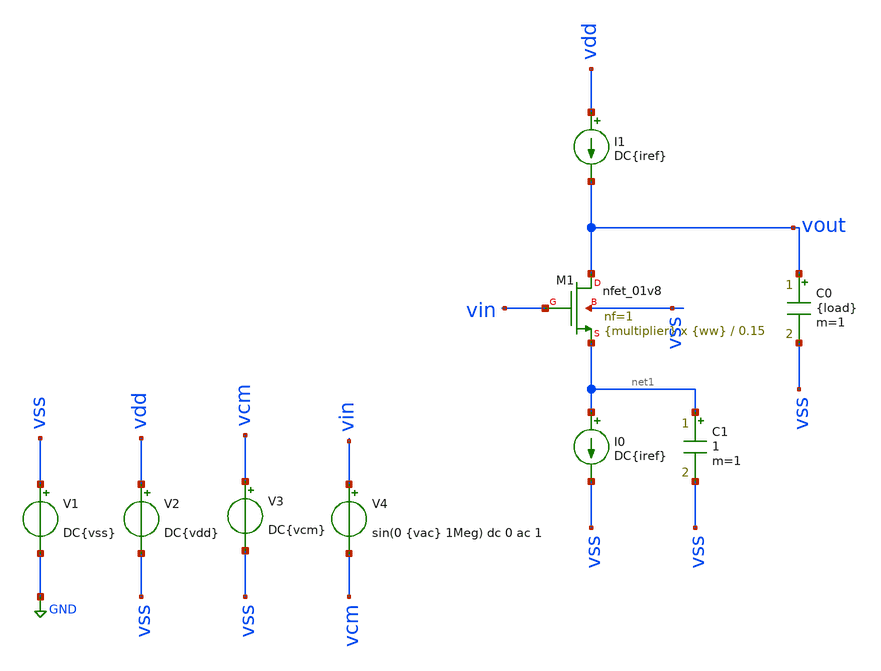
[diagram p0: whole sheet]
** sch_path: tp4/tp4.sch
**.subckt tp4
V1 vss GND DC{vss}
V2 vdd vss DC{vdd}
V3 vcm vss DC{vcm}
V4 vin vcm sin(0 {vac} 1Meg) dc 0 ac 1
XM1 vout vin net1 vss sky130_fd_pr__nfet_01v8 L=0.15 W={ww} nf=1 ad='int((nf+1)/2) * W/nf * 0.29' as='int((nf+2)/2) * W/nf * 0.29'
+ pd='2*int((nf+1)/2) * (W/nf + 0.29)' ps='2*int((nf+2)/2) * (W/nf + 0.29)' nrd='0.29 / W' nrs='0.29 / W'
+ sa=0 sb=0 sd=0 mult={multiplier} m={multiplier}
I0 net1 vss DC{iref}
C0 vout vss {load} m=1
I1 vdd vout DC{iref}
C1 net1 vss 1 m=1
**** begin user architecture code



* Circuit Parameters
.param iref = 100u
.param vdd  = 1.8
.param vss  = 0.0
.param vcm  = 0.9
.param vac  = 10m
.param multiplier = 1
.param load = 0.001f
.param ww = 0.45
.options TEMP = 65.0


* Models
*.lib ~/skywater/skywater-pdk/libraries/sky130_fd_pr_ngspice/latest/models/corners/sky130.lib TT
*.lib ~/skywater/skywater-pdk/libraries/sky130_fd_pr_ngspice/latest/models/corners/sky130.lib TT
.lib /foss/pdks/sky130A/libs.tech/ngspice/sky130.lib.spice tt
*.lib /foss/pdks/sky130A/libs.tech/ngspice/sky130.lib.spice.tt.red tt
* Data to save
.save all  @M.XM1.msky130_fd_pr__nfet_01v8[id]  @M.XM1.msky130_fd_pr__nfet_01v8[gm]  @M.XM1.msky130_fd_pr__nfet_01v8[gds]  @M.XM1.msky130_fd_pr__nfet_01v8[vth]  @M.XM1.msky130_fd_pr__nfet_01v8[vds]  @M.XM1.msky130_fd_pr__nfet_01v8[vdsat]  @M.XM1.msky130_fd_pr__nfet_01v8[vgs]  @M.XM1.msky130_fd_pr__nfet_01v8[cgs]  @M.XM1.msky130_fd_pr__nfet_01v8[cgd]  @M.XM1.msky130_fd_pr__nfet_01v8[cds]  @M.XM1.msky130_fd_pr__nfet_01v8[cgg]

* Simulation
.control

******************************************************
* analisis ruido w
******************************************************
alterparam multiplier = 5
alterparam load = 1f
reset
noise v(vout) V4 dec 100 10k 1000G 1
setplot noise1
plot onoise_spectrum ylog xlog
*plot inoise_spectrum onoise_spectrum ylog xlog

setplot noise2
print inoise_total
print onoise_total
print onoise_total.m.xm1.msky130_fd_pr__nfet_01v8.1overf
print onoise_total.m.xm1.msky130_fd_pr__nfet_01v8.id

set filetype=ascii
write tp4_noise.raw

******************************************************
* op
******************************************************
unset filetype
op
save all
write tp4.raw

.endc
.end


**** end user architecture code
**.ends
.GLOBAL GND
.end
